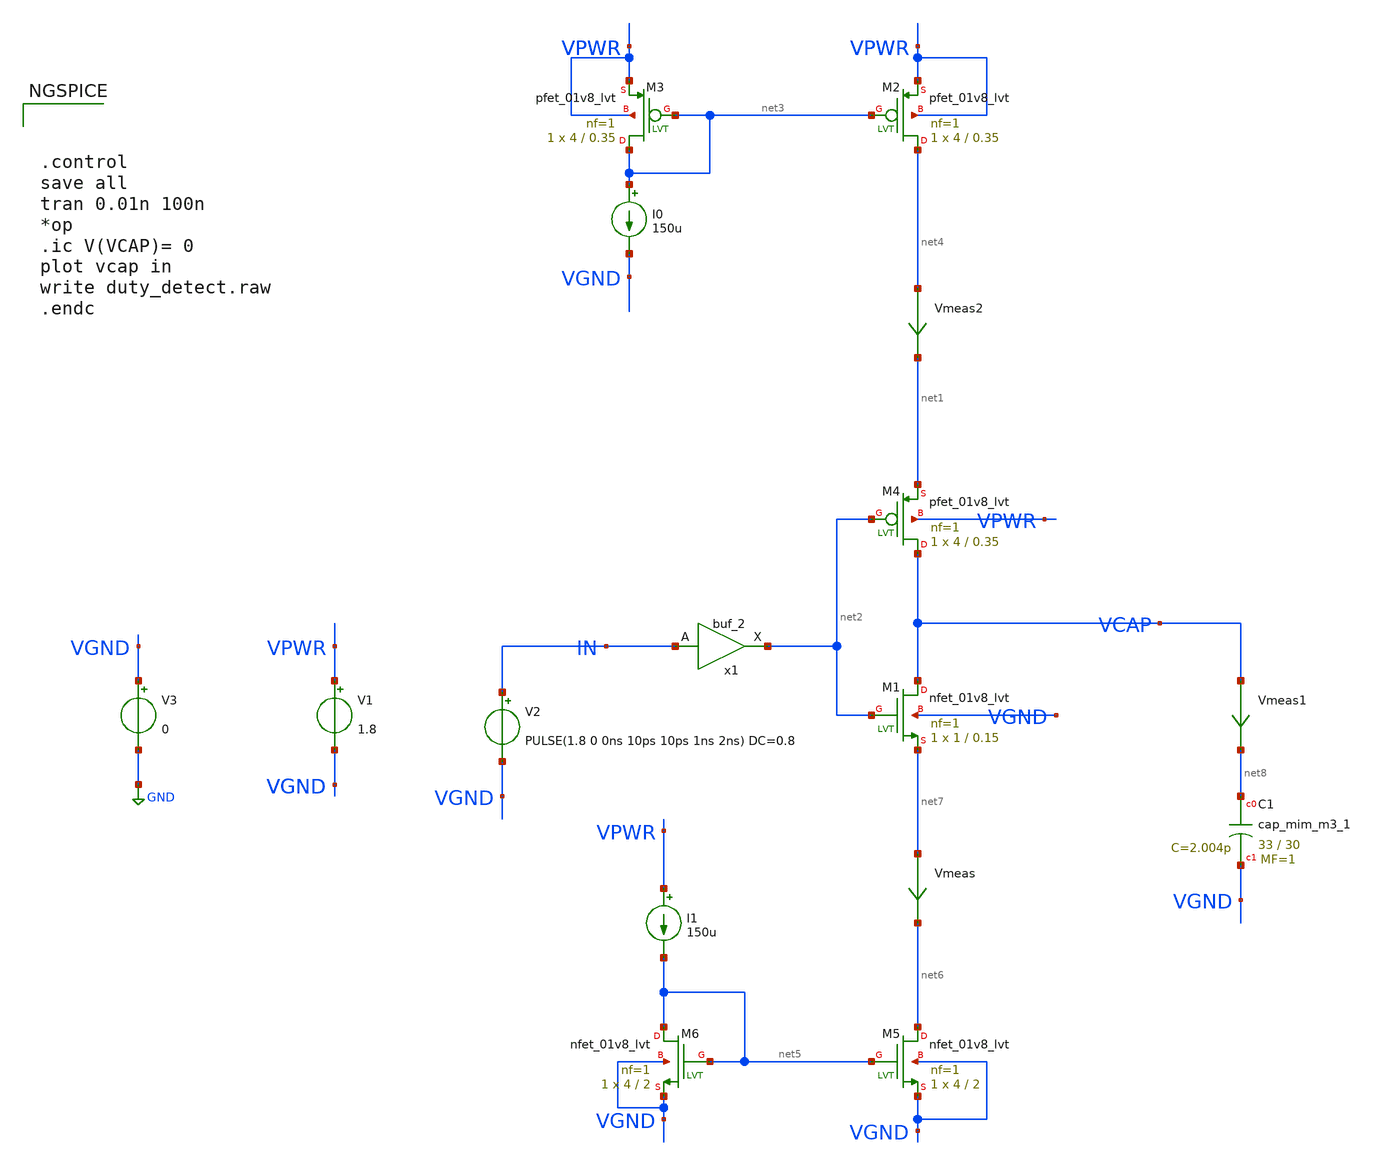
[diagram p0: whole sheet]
** sch_path: design/duty_detect.sch
**.subckt duty_detect
XM1 VCAP net2 net7 VGND sky130_fd_pr__nfet_01v8_lvt L=0.15 W=1 nf=1 ad='int((nf+1)/2) * W/nf * 0.29'
+ as='int((nf+2)/2) * W/nf * 0.29' pd='2*int((nf+1)/2) * (W/nf + 0.29)' ps='2*int((nf+2)/2) * (W/nf + 0.29)'
+ nrd='0.29 / W' nrs='0.29 / W' sa=0 sb=0 sd=0 mult=1 m=1
x1 IN VGND VNB VPB VPWR net2 sky130_fd_sc_hd__buf_2
I0 net3 VGND 150u
I1 VPWR net5 150u
XC1 net8 VGND sky130_fd_pr__cap_mim_m3_1 W=33 L=30 MF=1 m=1
V1 VPWR VGND 1.8
V2 IN VGND PULSE(1.8 0 0ns 10ps 10ps 1ns 2ns) DC=0.8
V3 VGND GND 0
XM5 net6 net5 VGND VGND sky130_fd_pr__nfet_01v8_lvt L=2 W=4 nf=1 ad='int((nf+1)/2) * W/nf * 0.29' as='int((nf+2)/2) * W/nf * 0.29'
+ pd='2*int((nf+1)/2) * (W/nf + 0.29)' ps='2*int((nf+2)/2) * (W/nf + 0.29)' nrd='0.29 / W' nrs='0.29 / W'
+ sa=0 sb=0 sd=0 mult=1 m=1
XM6 net5 net5 VGND VGND sky130_fd_pr__nfet_01v8_lvt L=2 W=4 nf=1 ad='int((nf+1)/2) * W/nf * 0.29' as='int((nf+2)/2) * W/nf * 0.29'
+ pd='2*int((nf+1)/2) * (W/nf + 0.29)' ps='2*int((nf+2)/2) * (W/nf + 0.29)' nrd='0.29 / W' nrs='0.29 / W'
+ sa=0 sb=0 sd=0 mult=1 m=1
XM2 net4 net3 VPWR VPWR sky130_fd_pr__pfet_01v8_lvt L=0.35 W=4 nf=1 ad='int((nf+1)/2) * W/nf * 0.29'
+ as='int((nf+2)/2) * W/nf * 0.29' pd='2*int((nf+1)/2) * (W/nf + 0.29)' ps='2*int((nf+2)/2) * (W/nf + 0.29)'
+ nrd='0.29 / W' nrs='0.29 / W' sa=0 sb=0 sd=0 mult=1 m=1
XM3 net3 net3 VPWR VPWR sky130_fd_pr__pfet_01v8_lvt L=0.35 W=4 nf=1 ad='int((nf+1)/2) * W/nf * 0.29'
+ as='int((nf+2)/2) * W/nf * 0.29' pd='2*int((nf+1)/2) * (W/nf + 0.29)' ps='2*int((nf+2)/2) * (W/nf + 0.29)'
+ nrd='0.29 / W' nrs='0.29 / W' sa=0 sb=0 sd=0 mult=1 m=1
XM4 VCAP net2 net1 VPWR sky130_fd_pr__pfet_01v8_lvt L=0.35 W=4 nf=1 ad='int((nf+1)/2) * W/nf * 0.29'
+ as='int((nf+2)/2) * W/nf * 0.29' pd='2*int((nf+1)/2) * (W/nf + 0.29)' ps='2*int((nf+2)/2) * (W/nf + 0.29)'
+ nrd='0.29 / W' nrs='0.29 / W' sa=0 sb=0 sd=0 mult=1 m=1
Vmeas net7 net6 0
.save i(vmeas)
Vmeas1 VCAP net8 0
.save i(vmeas1)
Vmeas2 net4 net1 0
.save i(vmeas2)
**** begin user architecture code

** opencircuitdesign pdks install
.lib $::SKYWATER_MODELS/sky130.lib.spice tt
.include $::SKYWATER_STDCELLS/sky130_fd_sc_hd.spice





.control
save all
tran 0.01n 100n
*op
.ic V(VCAP)= 0
plot vcap in
write duty_detect.raw
.endc


**** end user architecture code
**.ends
.GLOBAL GND
.end
